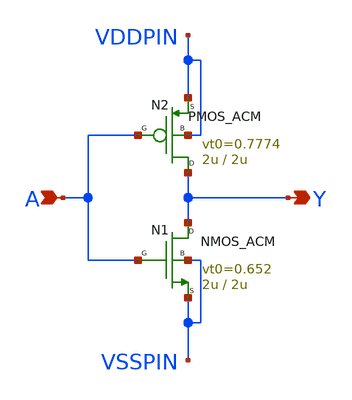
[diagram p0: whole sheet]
** sch_path: legacy/Examples/IHP-SG13/xschem/symbol/not_acm.sch
**.subckt not_acm A Y
*.ipin A
*.opin Y
N1 Y A VSSPIN VSSPIN NMOS_ACM w=2u l=2u n=1.38 is=67.3n vt0=0.652 sigma=20m zeta=5m
N2 Y A VDDPIN VDDPIN PMOS_ACM w=2u l=2u n=1.438 is=17.94n vt0=0.7774 sigma=20m zeta=5m
**.ends
.end
